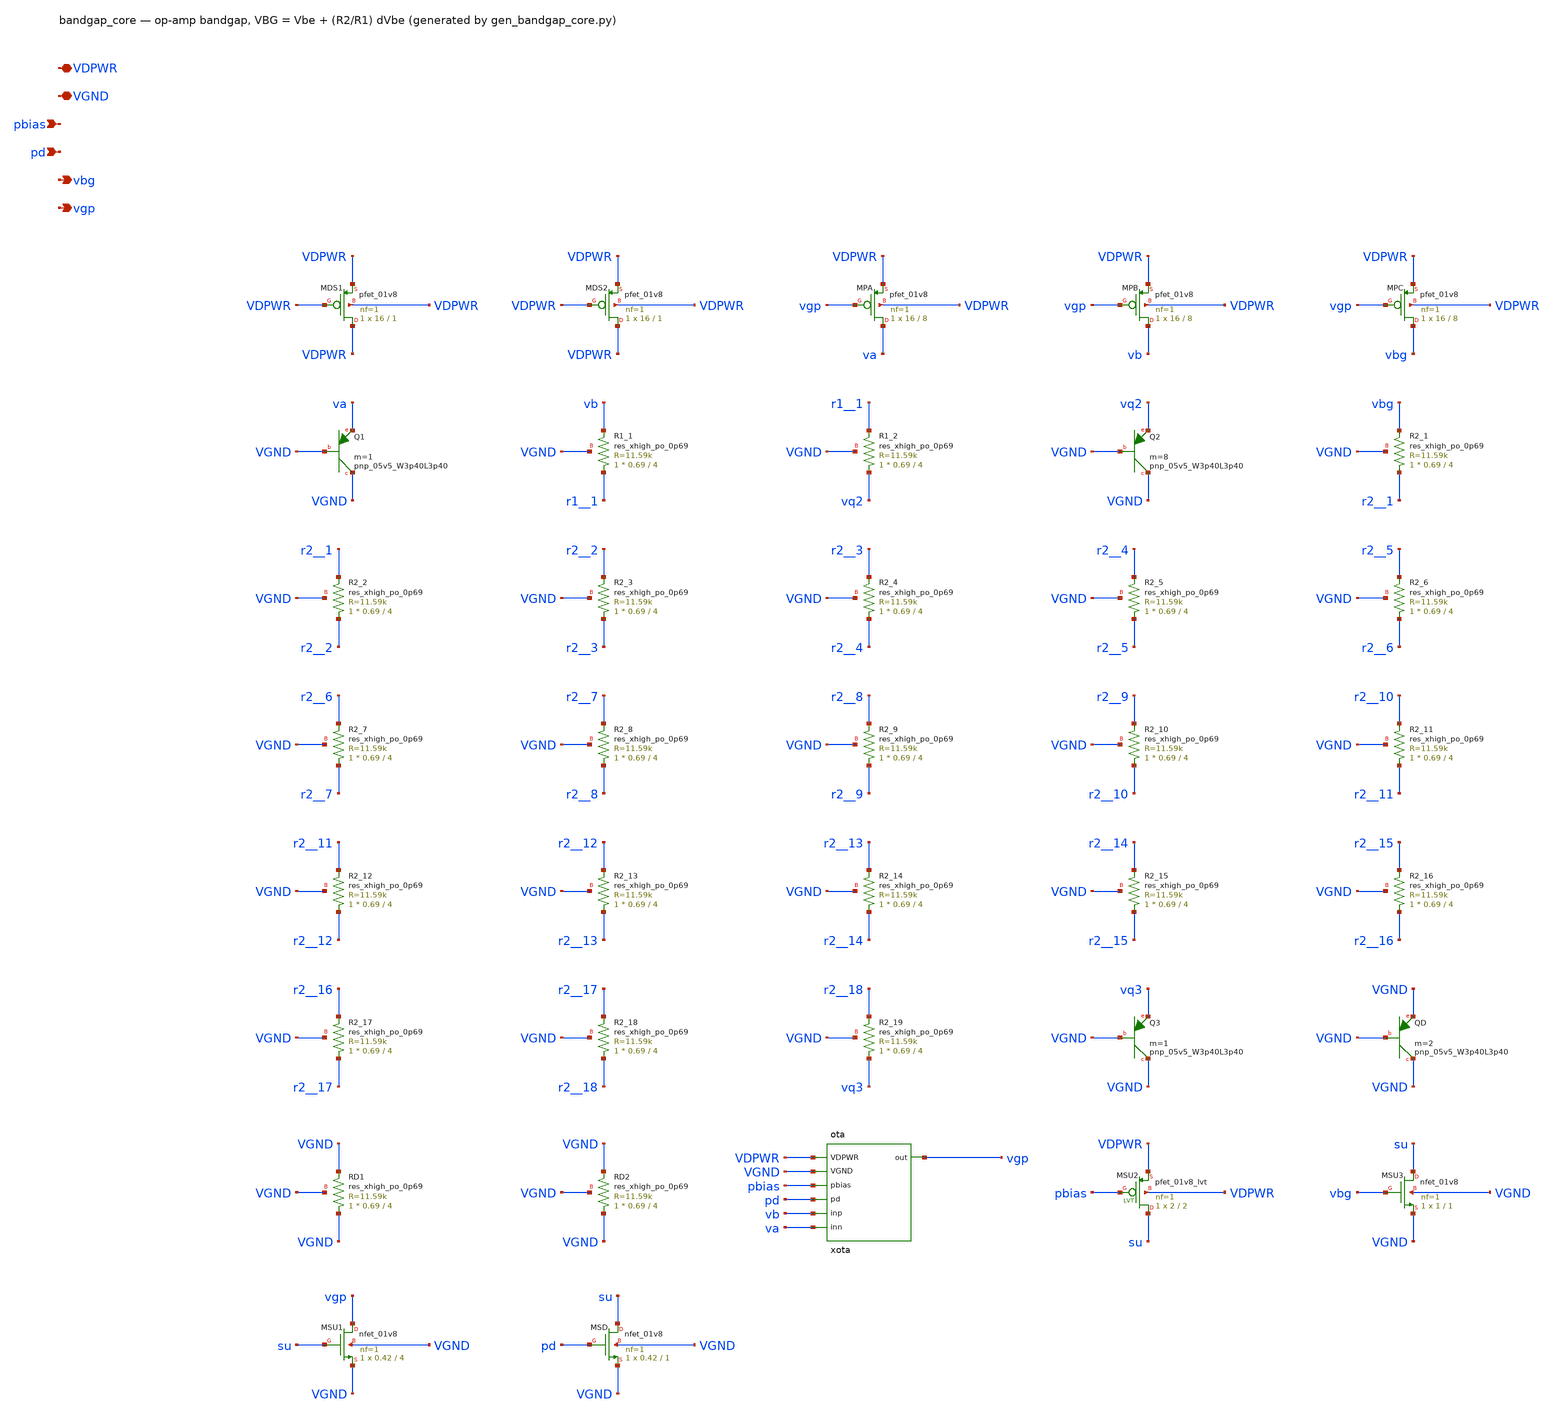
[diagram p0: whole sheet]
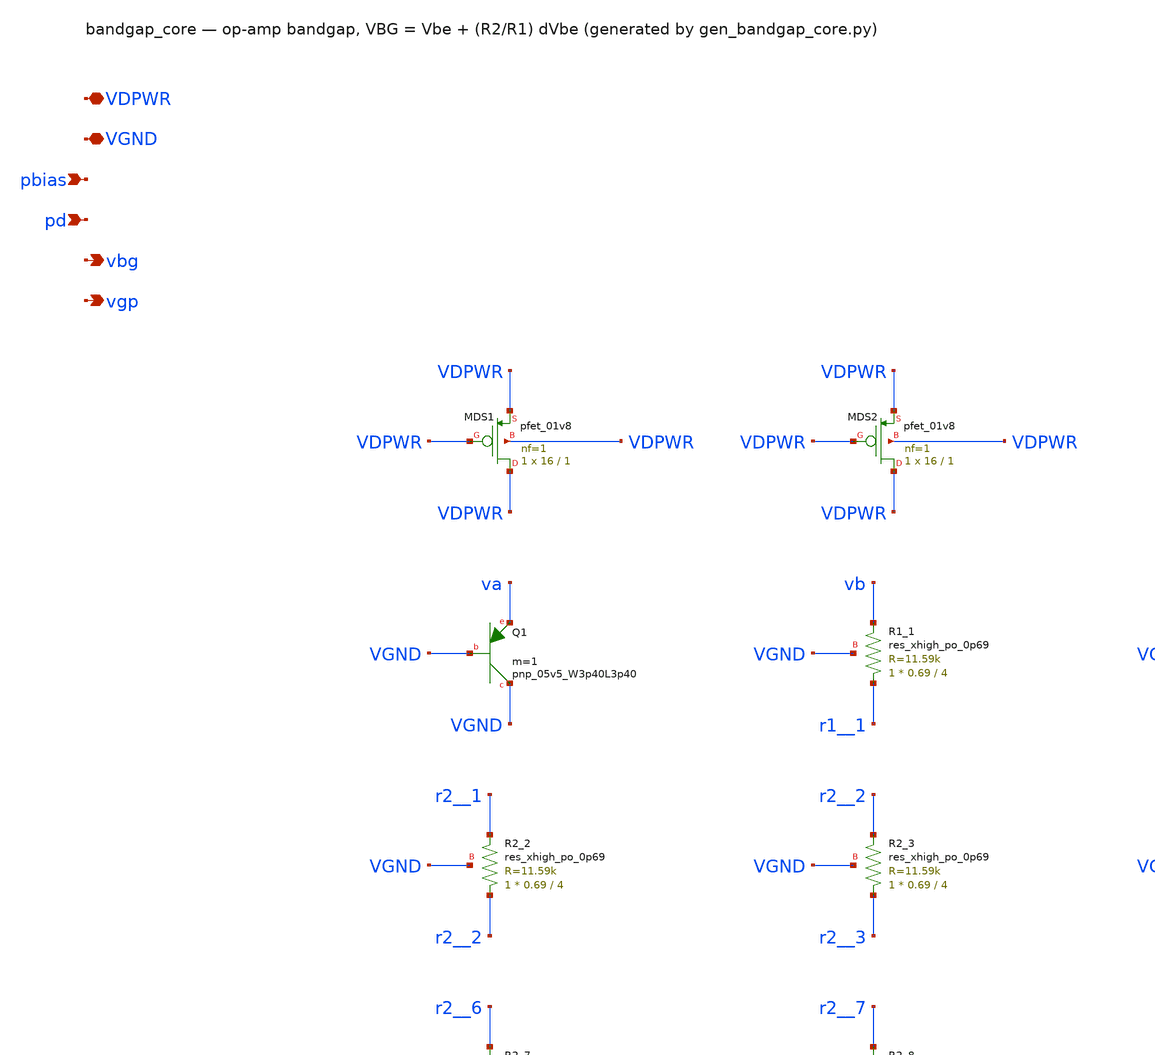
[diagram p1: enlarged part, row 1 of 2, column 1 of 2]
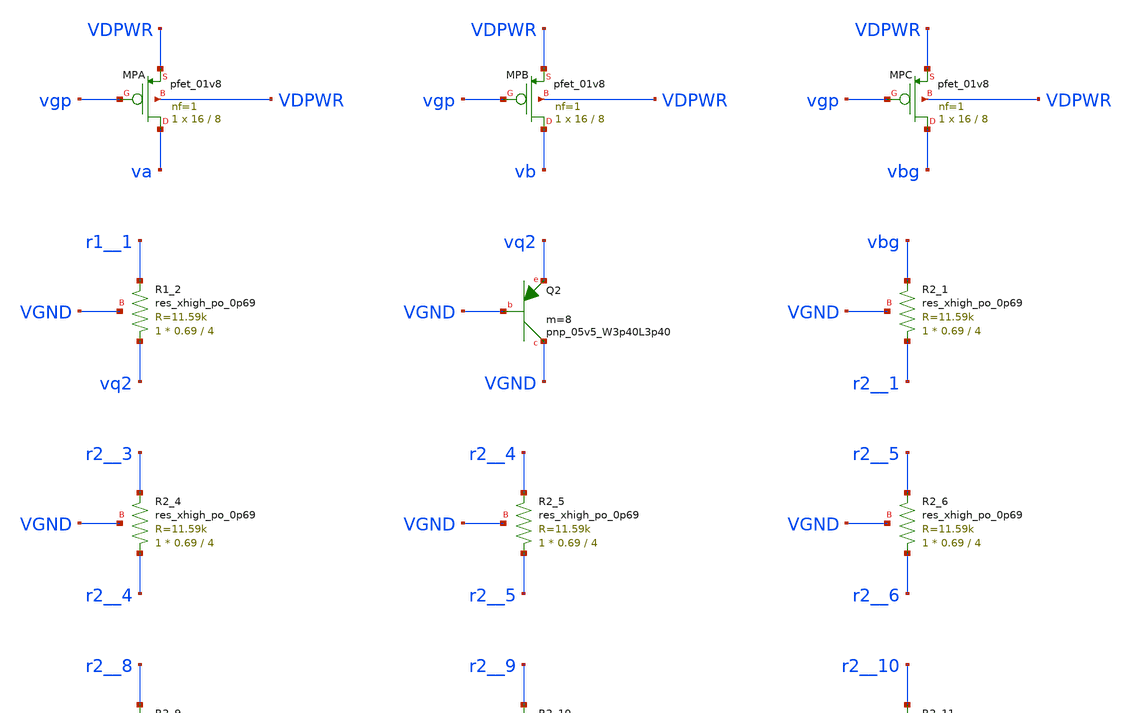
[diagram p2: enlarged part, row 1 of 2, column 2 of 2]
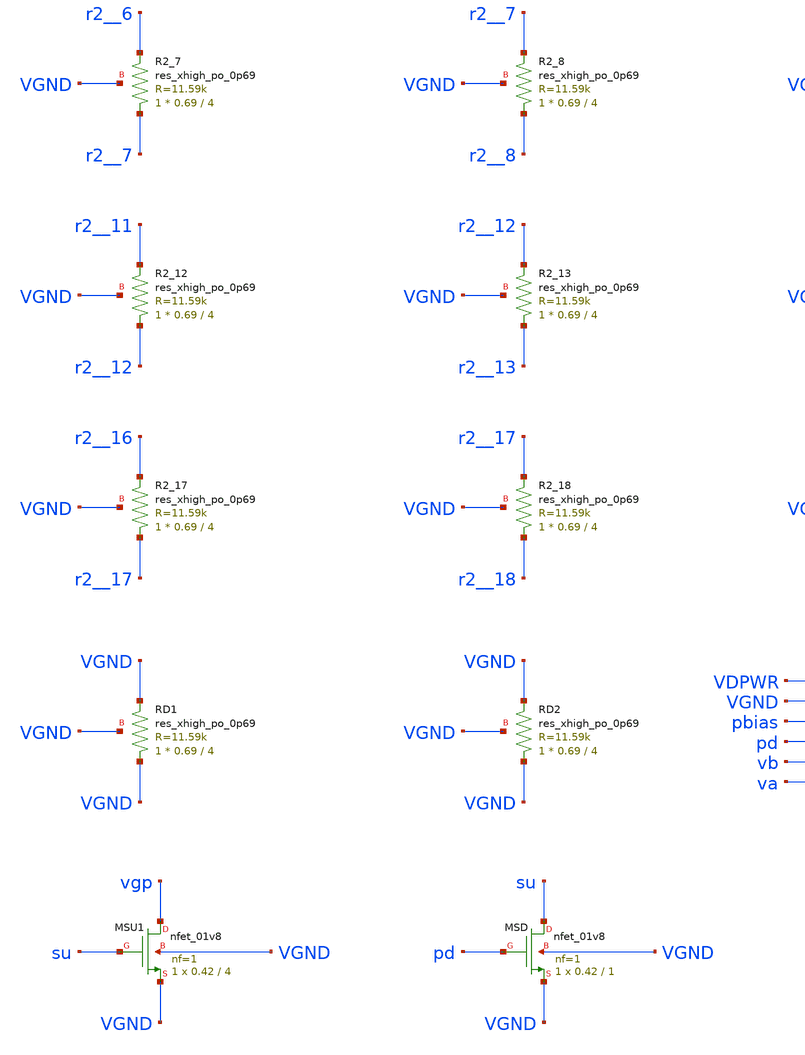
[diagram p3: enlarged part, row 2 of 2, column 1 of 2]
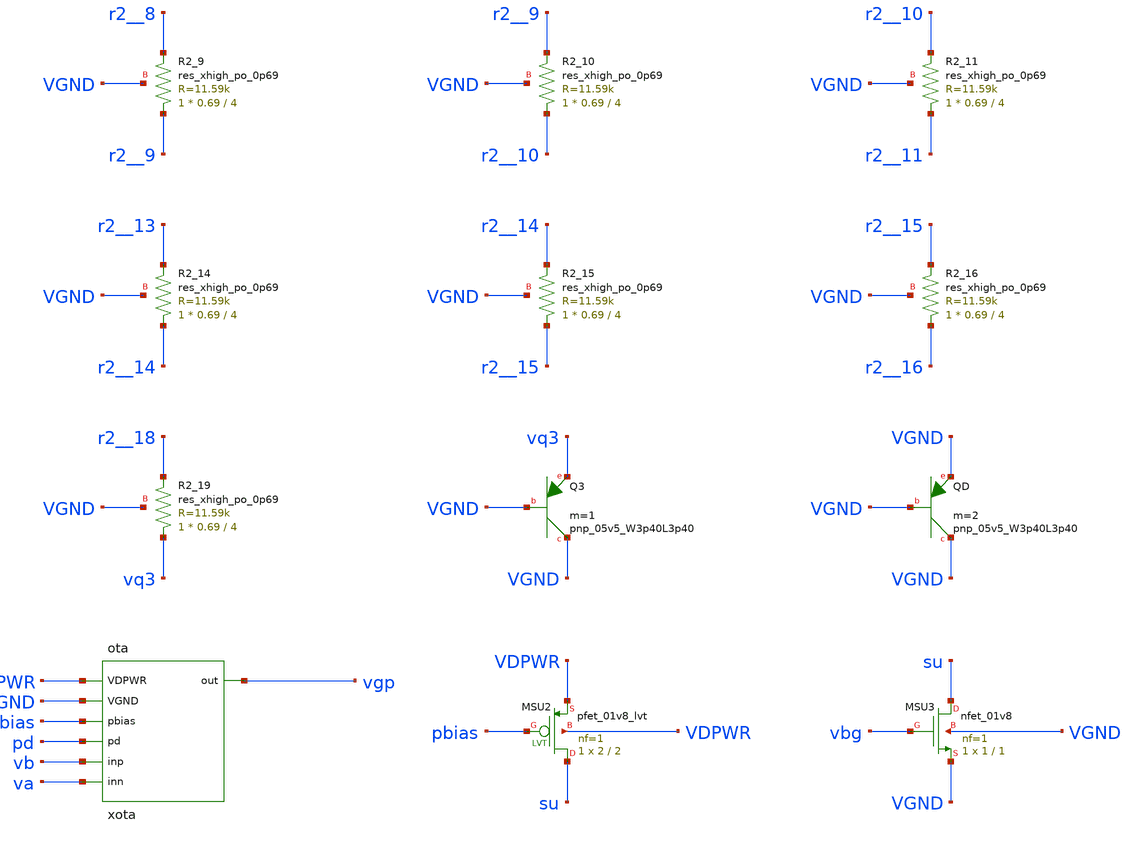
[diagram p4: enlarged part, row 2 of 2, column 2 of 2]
** sch_path: xschem/bandgap_core.sch
**.subckt bandgap_core VDPWR VGND pbias pd vbg vgp
*.iopin VDPWR
*.iopin VGND
*.ipin pbias
*.ipin pd
*.opin vbg
*.opin vgp
XMDS1 VDPWR VDPWR VDPWR VDPWR sky130_fd_pr__pfet_01v8 L=1 W=16 nf=1 ad='int((nf+1)/2) * W/nf * 0.29'
+ as='int((nf+2)/2) * W/nf * 0.29' pd='2*int((nf+1)/2) * (W/nf + 0.29)' ps='2*int((nf+2)/2) * (W/nf + 0.29)'
+ nrd='0.29 / W' nrs='0.29 / W' sa=0 sb=0 sd=0 mult=1 m=1
XMDS2 VDPWR VDPWR VDPWR VDPWR sky130_fd_pr__pfet_01v8 L=1 W=16 nf=1 ad='int((nf+1)/2) * W/nf * 0.29'
+ as='int((nf+2)/2) * W/nf * 0.29' pd='2*int((nf+1)/2) * (W/nf + 0.29)' ps='2*int((nf+2)/2) * (W/nf + 0.29)'
+ nrd='0.29 / W' nrs='0.29 / W' sa=0 sb=0 sd=0 mult=1 m=1
XMPA va vgp VDPWR VDPWR sky130_fd_pr__pfet_01v8 L=8 W=16 nf=1 ad='int((nf+1)/2) * W/nf * 0.29' as='int((nf+2)/2) * W/nf * 0.29'
+ pd='2*int((nf+1)/2) * (W/nf + 0.29)' ps='2*int((nf+2)/2) * (W/nf + 0.29)' nrd='0.29 / W' nrs='0.29 / W'
+ sa=0 sb=0 sd=0 mult=1 m=1
XMPB vb vgp VDPWR VDPWR sky130_fd_pr__pfet_01v8 L=8 W=16 nf=1 ad='int((nf+1)/2) * W/nf * 0.29' as='int((nf+2)/2) * W/nf * 0.29'
+ pd='2*int((nf+1)/2) * (W/nf + 0.29)' ps='2*int((nf+2)/2) * (W/nf + 0.29)' nrd='0.29 / W' nrs='0.29 / W'
+ sa=0 sb=0 sd=0 mult=1 m=1
XMPC vbg vgp VDPWR VDPWR sky130_fd_pr__pfet_01v8 L=8 W=16 nf=1 ad='int((nf+1)/2) * W/nf * 0.29' as='int((nf+2)/2) * W/nf * 0.29'
+ pd='2*int((nf+1)/2) * (W/nf + 0.29)' ps='2*int((nf+2)/2) * (W/nf + 0.29)' nrd='0.29 / W' nrs='0.29 / W'
+ sa=0 sb=0 sd=0 mult=1 m=1
XQ1 VGND VGND va sky130_fd_pr__pnp_05v5_W3p40L3p40 m=1
XR1_1 r1__1 vb VGND sky130_fd_pr__res_xhigh_po_0p69 L=4 mult=1 m=1
XR1_2 vq2 r1__1 VGND sky130_fd_pr__res_xhigh_po_0p69 L=4 mult=1 m=1
XQ2 VGND VGND vq2 sky130_fd_pr__pnp_05v5_W3p40L3p40 m=8
XR2_1 r2__1 vbg VGND sky130_fd_pr__res_xhigh_po_0p69 L=4 mult=1 m=1
XR2_2 r2__2 r2__1 VGND sky130_fd_pr__res_xhigh_po_0p69 L=4 mult=1 m=1
XR2_3 r2__3 r2__2 VGND sky130_fd_pr__res_xhigh_po_0p69 L=4 mult=1 m=1
XR2_4 r2__4 r2__3 VGND sky130_fd_pr__res_xhigh_po_0p69 L=4 mult=1 m=1
XR2_5 r2__5 r2__4 VGND sky130_fd_pr__res_xhigh_po_0p69 L=4 mult=1 m=1
XR2_6 r2__6 r2__5 VGND sky130_fd_pr__res_xhigh_po_0p69 L=4 mult=1 m=1
XR2_7 r2__7 r2__6 VGND sky130_fd_pr__res_xhigh_po_0p69 L=4 mult=1 m=1
XR2_8 r2__8 r2__7 VGND sky130_fd_pr__res_xhigh_po_0p69 L=4 mult=1 m=1
XR2_9 r2__9 r2__8 VGND sky130_fd_pr__res_xhigh_po_0p69 L=4 mult=1 m=1
XR2_10 r2__10 r2__9 VGND sky130_fd_pr__res_xhigh_po_0p69 L=4 mult=1 m=1
XR2_11 r2__11 r2__10 VGND sky130_fd_pr__res_xhigh_po_0p69 L=4 mult=1 m=1
XR2_12 r2__12 r2__11 VGND sky130_fd_pr__res_xhigh_po_0p69 L=4 mult=1 m=1
XR2_13 r2__13 r2__12 VGND sky130_fd_pr__res_xhigh_po_0p69 L=4 mult=1 m=1
XR2_14 r2__14 r2__13 VGND sky130_fd_pr__res_xhigh_po_0p69 L=4 mult=1 m=1
XR2_15 r2__15 r2__14 VGND sky130_fd_pr__res_xhigh_po_0p69 L=4 mult=1 m=1
XR2_16 r2__16 r2__15 VGND sky130_fd_pr__res_xhigh_po_0p69 L=4 mult=1 m=1
XR2_17 r2__17 r2__16 VGND sky130_fd_pr__res_xhigh_po_0p69 L=4 mult=1 m=1
XR2_18 r2__18 r2__17 VGND sky130_fd_pr__res_xhigh_po_0p69 L=4 mult=1 m=1
XR2_19 vq3 r2__18 VGND sky130_fd_pr__res_xhigh_po_0p69 L=4 mult=1 m=1
XQ3 VGND VGND vq3 sky130_fd_pr__pnp_05v5_W3p40L3p40 m=1
XQD VGND VGND VGND sky130_fd_pr__pnp_05v5_W3p40L3p40 m=2
XRD1 VGND VGND VGND sky130_fd_pr__res_xhigh_po_0p69 L=4 mult=1 m=1
XRD2 VGND VGND VGND sky130_fd_pr__res_xhigh_po_0p69 L=4 mult=1 m=1
xota VDPWR VGND pbias pd vb va vgp ota
XMSU2 su pbias VDPWR VDPWR sky130_fd_pr__pfet_01v8_lvt L=2 W=2 nf=1 ad='int((1 + 1)/2) * 2 / 1 * 0.29'
+ as='int((1 + 2)/2) * 2 / 1 * 0.29' pd='2*int((1 + 1)/2) * (2 / 1 + 0.29)' ps='2*int((1 + 2)/2) * (2 / 1 + 0.29)'
+ nrd='0.29 / 2 ' nrs='0.29 / 2 ' sa=0 sb=0 sd=0 mult=1 m=1
XMSU3 su vbg VGND VGND sky130_fd_pr__nfet_01v8 L=1 W=1 nf=1 ad='int((1 + 1)/2) * 1 / 1 * 0.29' as='int((1 + 2)/2) * 1 / 1 * 0.29'
+ pd='2*int((1 + 1)/2) * (1 / 1 + 0.29)' ps='2*int((1 + 2)/2) * (1 / 1 + 0.29)' nrd='0.29 / 1 ' nrs='0.29 / 1 '
+ sa=0 sb=0 sd=0 mult=1 m=1
XMSU1 vgp su VGND VGND sky130_fd_pr__nfet_01v8 L=4 W=0.42 nf=1 ad='int((1 + 1)/2) * 0.42 / 1 * 0.29'
+ as='int((1 + 2)/2) * 0.42 / 1 * 0.29' pd='2*int((1 + 1)/2) * (0.42 / 1 + 0.29)' ps='2*int((1 + 2)/2) * (0.42 / 1 + 0.29)'
+ nrd='0.29 / 0.42 ' nrs='0.29 / 0.42 ' sa=0 sb=0 sd=0 mult=1 m=1
XMSD su pd VGND VGND sky130_fd_pr__nfet_01v8 L=1 W=0.42 nf=1 ad='int((1 + 1)/2) * 0.42 / 1 * 0.29' as='int((1 + 2)/2) * 0.42 / 1 * 0.29'
+ pd='2*int((1 + 1)/2) * (0.42 / 1 + 0.29)' ps='2*int((1 + 2)/2) * (0.42 / 1 + 0.29)' nrd='0.29 / 0.42 '
+ nrs='0.29 / 0.42 ' sa=0 sb=0 sd=0 mult=1 m=1
**.ends

* expanding   symbol:  ota.sym # of pins=7
** sym_path: xschem/ota.sym
** sch_path: xschem/ota.sch
.subckt ota VDPWR VGND pbias pd inp inn out
*.iopin VDPWR
*.iopin VGND
*.ipin pbias
*.ipin pd
*.ipin inp
*.ipin inn
*.opin out
XM5 tail pbias VDPWR VDPWR sky130_fd_pr__pfet_01v8_lvt L=2 W=2 nf=1 ad='int((1 + 1)/2) * 2 / 1 * 0.29'
+ as='int((1 + 2)/2) * 2 / 1 * 0.29' pd='2*int((1 + 1)/2) * (2 / 1 + 0.29)' ps='2*int((1 + 2)/2) * (2 / 1 + 0.29)'
+ nrd='0.29 / 2 ' nrs='0.29 / 2 ' sa=0 sb=0 sd=0 mult=2 m=2
XM1 d1 inn tail VDPWR sky130_fd_pr__pfet_01v8_lvt L=8 W=32 nf=1 ad='int((1 + 1)/2) * 32 / 1 * 0.29' as='int((1 + 2)/2) * 32 / 1 * 0.29'
+ pd='2*int((1 + 1)/2) * (32 / 1 + 0.29)' ps='2*int((1 + 2)/2) * (32 / 1 + 0.29)' nrd='0.29 / 32 ' nrs='0.29 / 32 '
+ sa=0 sb=0 sd=0 mult=1 m=1
XM2 out1 inp tail VDPWR sky130_fd_pr__pfet_01v8_lvt L=8 W=32 nf=1 ad='int((1 + 1)/2) * 32 / 1 * 0.29'
+ as='int((1 + 2)/2) * 32 / 1 * 0.29' pd='2*int((1 + 1)/2) * (32 / 1 + 0.29)' ps='2*int((1 + 2)/2) * (32 / 1 + 0.29)'
+ nrd='0.29 / 32 ' nrs='0.29 / 32 ' sa=0 sb=0 sd=0 mult=1 m=1
XM3 d1 d1 VGND VGND sky130_fd_pr__nfet_01v8 L=16 W=4 nf=1 ad='int((1 + 1)/2) * 4 / 1 * 0.29' as='int((1 + 2)/2) * 4 / 1 * 0.29'
+ pd='2*int((1 + 1)/2) * (4 / 1 + 0.29)' ps='2*int((1 + 2)/2) * (4 / 1 + 0.29)' nrd='0.29 / 4 ' nrs='0.29 / 4 '
+ sa=0 sb=0 sd=0 mult=1 m=1
XM4 out1 d1 VGND VGND sky130_fd_pr__nfet_01v8 L=16 W=4 nf=1 ad='int((1 + 1)/2) * 4 / 1 * 0.29' as='int((1 + 2)/2) * 4 / 1 * 0.29'
+ pd='2*int((1 + 1)/2) * (4 / 1 + 0.29)' ps='2*int((1 + 2)/2) * (4 / 1 + 0.29)' nrd='0.29 / 4 ' nrs='0.29 / 4 '
+ sa=0 sb=0 sd=0 mult=1 m=1
XM6 out out1 VGND VGND sky130_fd_pr__nfet_01v8 L=16 W=4 nf=1 ad='int((1 + 1)/2) * 4 / 1 * 0.29' as='int((1 + 2)/2) * 4 / 1 * 0.29'
+ pd='2*int((1 + 1)/2) * (4 / 1 + 0.29)' ps='2*int((1 + 2)/2) * (4 / 1 + 0.29)' nrd='0.29 / 4 ' nrs='0.29 / 4 '
+ sa=0 sb=0 sd=0 mult=4 m=4
XM7 out pbias VDPWR VDPWR sky130_fd_pr__pfet_01v8_lvt L=2 W=2 nf=1 ad='int((1 + 1)/2) * 2 / 1 * 0.29'
+ as='int((1 + 2)/2) * 2 / 1 * 0.29' pd='2*int((1 + 1)/2) * (2 / 1 + 0.29)' ps='2*int((1 + 2)/2) * (2 / 1 + 0.29)'
+ nrd='0.29 / 2 ' nrs='0.29 / 2 ' sa=0 sb=0 sd=0 mult=4 m=4
XRZA rzm out1 VGND sky130_fd_pr__res_xhigh_po_0p35 L=10.45 mult=1 m=1
XRZB cz rzm VGND sky130_fd_pr__res_xhigh_po_0p35 L=10.45 mult=1 m=1
XRZD1 VGND VGND VGND sky130_fd_pr__res_xhigh_po_0p35 L=10.45 mult=1 m=1
XRZD2 VGND VGND VGND sky130_fd_pr__res_xhigh_po_0p35 L=10.45 mult=1 m=1
XCC cz out sky130_fd_pr__cap_mim_m3_1 W=16 L=16 MF=4 m=4
XMDP1 VDPWR VDPWR VDPWR VDPWR sky130_fd_pr__pfet_01v8_lvt L=1 W=16 nf=1 ad='int((1 + 1)/2) * 16 / 1 * 0.29'
+ as='int((1 + 2)/2) * 16 / 1 * 0.29' pd='2*int((1 + 1)/2) * (16 / 1 + 0.29)' ps='2*int((1 + 2)/2) * (16 / 1 + 0.29)'
+ nrd='0.29 / 16 ' nrs='0.29 / 16 ' sa=0 sb=0 sd=0 mult=1 m=1
XMDP2 VDPWR VDPWR VDPWR VDPWR sky130_fd_pr__pfet_01v8_lvt L=1 W=16 nf=1 ad='int((1 + 1)/2) * 16 / 1 * 0.29'
+ as='int((1 + 2)/2) * 16 / 1 * 0.29' pd='2*int((1 + 1)/2) * (16 / 1 + 0.29)' ps='2*int((1 + 2)/2) * (16 / 1 + 0.29)'
+ nrd='0.29 / 16 ' nrs='0.29 / 16 ' sa=0 sb=0 sd=0 mult=1 m=1
XMPD out pdb VDPWR VDPWR sky130_fd_pr__pfet_01v8 L=1 W=0.42 nf=1 ad='int((nf+1)/2) * W/nf * 0.29' as='int((nf+2)/2) * W/nf * 0.29'
+ pd='2*int((nf+1)/2) * (W/nf + 0.29)' ps='2*int((nf+2)/2) * (W/nf + 0.29)' nrd='0.29 / W' nrs='0.29 / W'
+ sa=0 sb=0 sd=0 mult=1 m=1
XMND out1 pd VGND VGND sky130_fd_pr__nfet_01v8 L=1 W=0.42 nf=1 ad='int((1 + 1)/2) * 0.42 / 1 * 0.29'
+ as='int((1 + 2)/2) * 0.42 / 1 * 0.29' pd='2*int((1 + 1)/2) * (0.42 / 1 + 0.29)' ps='2*int((1 + 2)/2) * (0.42 / 1 + 0.29)'
+ nrd='0.29 / 0.42 ' nrs='0.29 / 0.42 ' sa=0 sb=0 sd=0 mult=1 m=1
XMIP pdb pd VDPWR VDPWR sky130_fd_pr__pfet_01v8 L=1 W=0.84 nf=1 ad='int((nf+1)/2) * W/nf * 0.29' as='int((nf+2)/2) * W/nf * 0.29'
+ pd='2*int((nf+1)/2) * (W/nf + 0.29)' ps='2*int((nf+2)/2) * (W/nf + 0.29)' nrd='0.29 / W' nrs='0.29 / W'
+ sa=0 sb=0 sd=0 mult=1 m=1
XMIN pdb pd VGND VGND sky130_fd_pr__nfet_01v8 L=1 W=0.42 nf=1 ad='int((1 + 1)/2) * 0.42 / 1 * 0.29' as='int((1 + 2)/2) * 0.42 / 1 * 0.29'
+ pd='2*int((1 + 1)/2) * (0.42 / 1 + 0.29)' ps='2*int((1 + 2)/2) * (0.42 / 1 + 0.29)' nrd='0.29 / 0.42 '
+ nrs='0.29 / 0.42 ' sa=0 sb=0 sd=0 mult=1 m=1
.ends

.end
